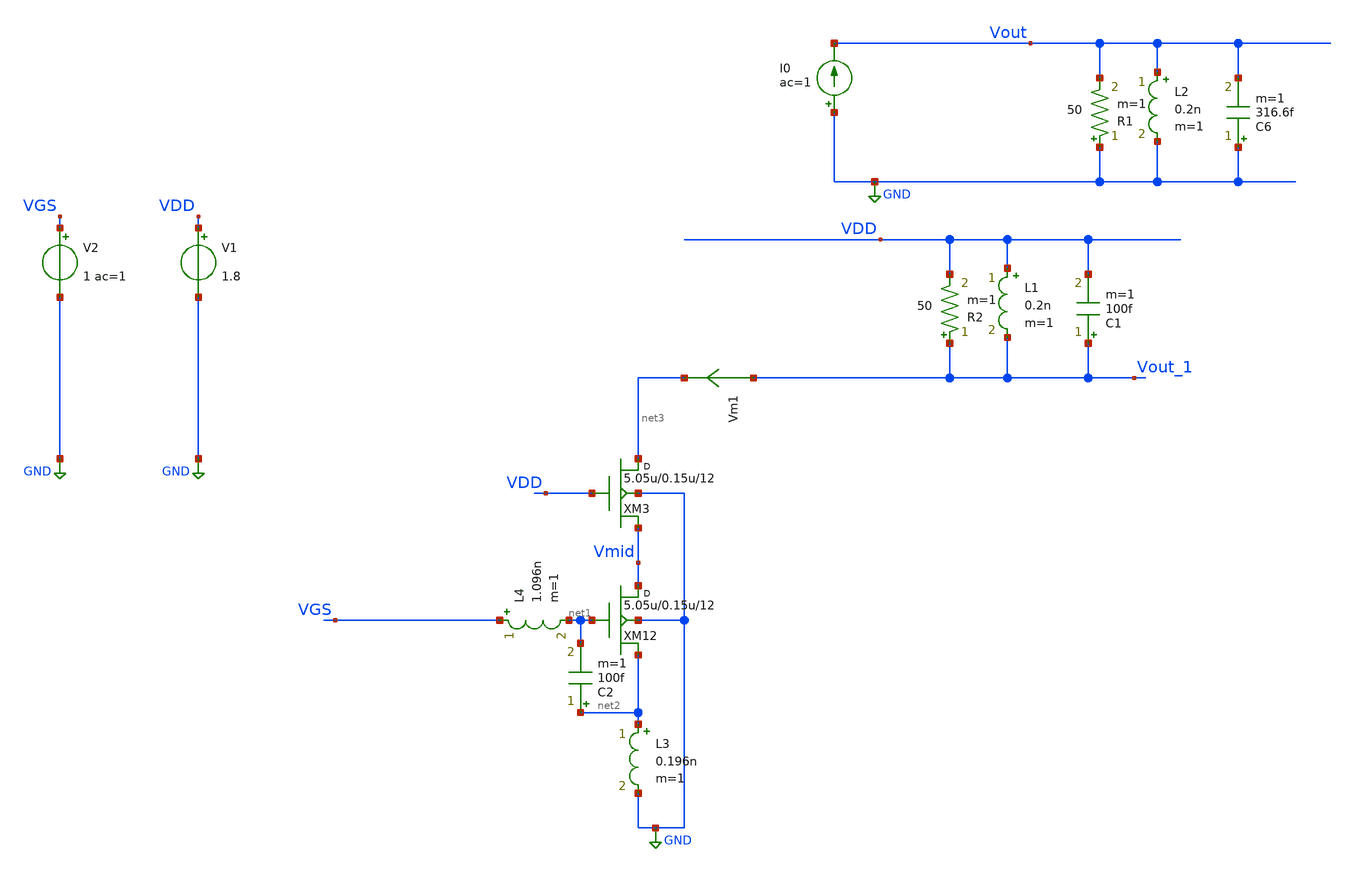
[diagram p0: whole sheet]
** sch_path: xschem/lna/Input.sch
**.subckt Input
I0 GND Vout ac=1
L2 Vout GND 0.2n m=1
C6 GND Vout 316.6f m=1
R1 GND Vout 50 m=1
XM12 Vmid net1 net2 GND sky130_fd_pr__rf_nfet_01v8_bM04W5p00L0p15_ext w=5.05u l=0.15u m=12
L1 VDD Vout_1 0.2n m=1
C1 Vout_1 VDD 100f m=1
R2 Vout_1 VDD 50 m=1
V1 VDD GND 1.8
V2 VGS GND 1 ac=1
XM3 net3 VDD Vmid GND sky130_fd_pr__rf_nfet_01v8_bM04W5p00L0p15_ext w=5.05u l=0.15u m=12
Vm1 Vout_1 net3 0
.save i(vm1)
L3 net2 GND 0.196n m=1
L4 VGS net1 1.096n m=1
C2 net2 net1 100f m=1
**** begin user architecture code


.subckt sky130_fd_pr__rf_nfet_01v8_bM04W5p00L0p15_ext DRAIN GATE SOURCE SUBSTRATE
X0 DRAIN GATE SOURCE SUBSTRATE sky130_fd_pr__nfet_01v8 ad=2.828e+12p pd=2.132e+07u as=4.242e+12p
+ ps=3.198e+07u w=5.05e+06u l=150000u
X1 SOURCE SUBSTRATE SUBSTRATE SUBSTRATE sky130_fd_pr__nfet_01v8 ad=0p pd=0u as=3.03e+12p
+ ps=2.14e+07u w=5.05e+06u l=150000u
X2 SOURCE GATE DRAIN SUBSTRATE sky130_fd_pr__nfet_01v8 ad=0p pd=0u as=0p ps=0u w=5.05e+06u l=150000u
X3 DRAIN GATE SOURCE SUBSTRATE sky130_fd_pr__nfet_01v8 ad=0p pd=0u as=0p ps=0u w=5.05e+06u l=150000u
X4 SUBSTRATE SUBSTRATE SOURCE SUBSTRATE sky130_fd_pr__nfet_01v8 ad=0p pd=0u as=0p ps=0u w=5.05e+06u
+ l=150000u
X5 SOURCE GATE DRAIN SUBSTRATE sky130_fd_pr__nfet_01v8 ad=0p pd=0u as=0p ps=0u w=5.05e+06u l=150000u
.ends
*.sp dec 1000 0.1e9 100e9 1
*.ac dec 1000 0.01e9 100e9
.option GMIN=1e-15
.control
save all
run
display

ac dec 10 1G 100G

plot Vout_1
plot abs(real(Vout_1))
plot imag(Vout_1)
plot vm1#branch

.endc



** opencircuitdesign pdks install
.lib $::SKYWATER_MODELS/sky130.lib.spice tt


**** end user architecture code
**.ends
.GLOBAL GND
.end
